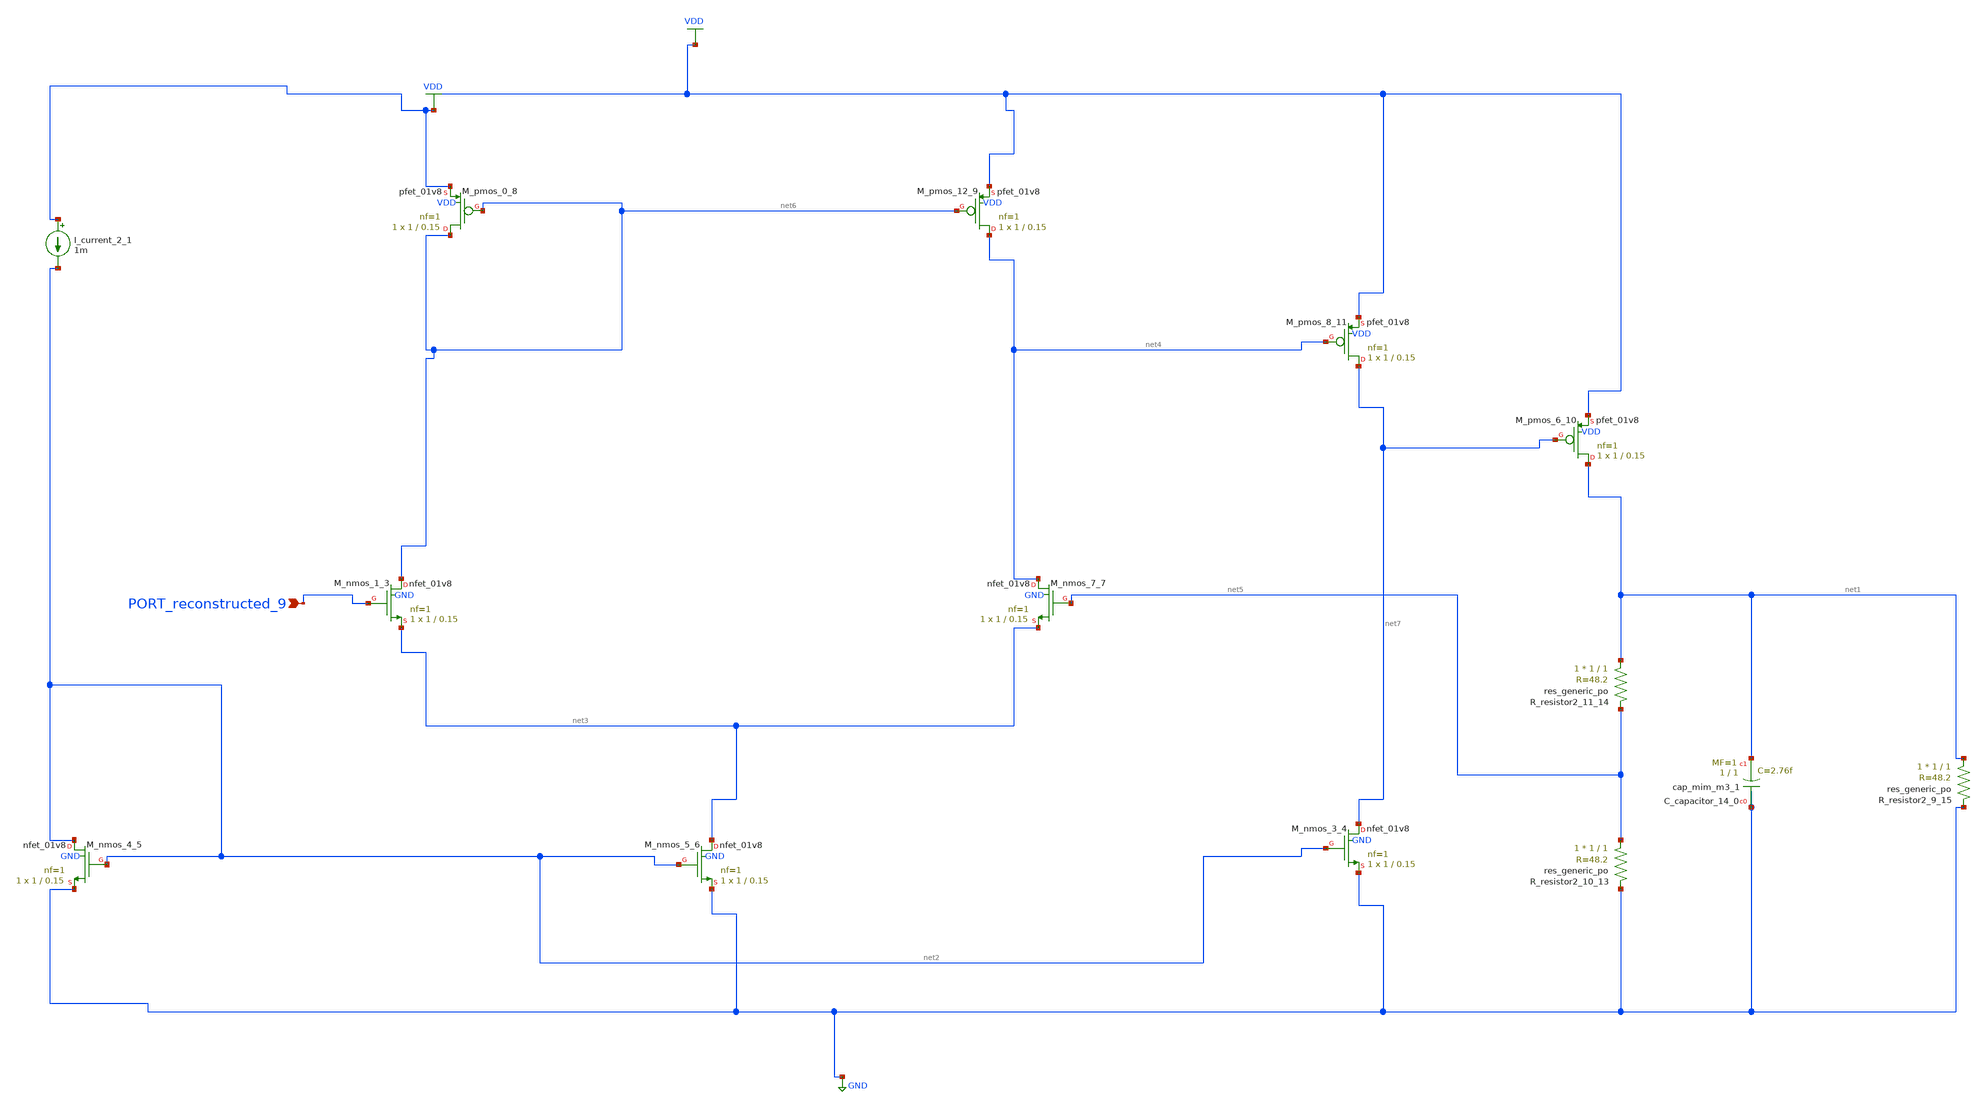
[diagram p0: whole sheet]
** sch_path: schematics/10_1007_s10470-009-9299-5_04_001_crop1.sch
**.subckt 10_1007_s10470-009-9299-5_04_001_crop1 PORT_reconstructed_9
*.ipin PORT_reconstructed_9
XC_capacitor_14_0 GND net1 sky130_fd_pr__cap_mim_m3_1 W=1 L=1 MF=1 m=1
I_current_2_1 VDD net2 1m
XM_nmos_1_3 net6 PORT_reconstructed_9 net3 GND sky130_fd_pr__nfet_01v8 L=0.15 W=1 nf=1 ad='int((1 + 1)/2) * 1 / 1 * 0.29'
+ as='int((1 + 2)/2) * 1 / 1 * 0.29' pd='2*int((1 + 1)/2) * (1 / 1 + 0.29)' ps='2*int((1 + 2)/2) * (1 / 1 + 0.29)'
+ nrd='0.29 / 1 ' nrs='0.29 / 1 ' sa=0 sb=0 sd=0 mult=1 m=1
XM_nmos_3_4 net7 net2 GND GND sky130_fd_pr__nfet_01v8 L=0.15 W=1 nf=1 ad='int((1 + 1)/2) * 1 / 1 * 0.29'
+ as='int((1 + 2)/2) * 1 / 1 * 0.29' pd='2*int((1 + 1)/2) * (1 / 1 + 0.29)' ps='2*int((1 + 2)/2) * (1 / 1 + 0.29)'
+ nrd='0.29 / 1 ' nrs='0.29 / 1 ' sa=0 sb=0 sd=0 mult=1 m=1
XM_nmos_4_5 net2 net2 GND GND sky130_fd_pr__nfet_01v8 L=0.15 W=1 nf=1 ad='int((1 + 1)/2) * 1 / 1 * 0.29'
+ as='int((1 + 2)/2) * 1 / 1 * 0.29' pd='2*int((1 + 1)/2) * (1 / 1 + 0.29)' ps='2*int((1 + 2)/2) * (1 / 1 + 0.29)'
+ nrd='0.29 / 1 ' nrs='0.29 / 1 ' sa=0 sb=0 sd=0 mult=1 m=1
XM_nmos_5_6 net3 net2 GND GND sky130_fd_pr__nfet_01v8 L=0.15 W=1 nf=1 ad='int((1 + 1)/2) * 1 / 1 * 0.29'
+ as='int((1 + 2)/2) * 1 / 1 * 0.29' pd='2*int((1 + 1)/2) * (1 / 1 + 0.29)' ps='2*int((1 + 2)/2) * (1 / 1 + 0.29)'
+ nrd='0.29 / 1 ' nrs='0.29 / 1 ' sa=0 sb=0 sd=0 mult=1 m=1
XM_nmos_7_7 net4 net5 net3 GND sky130_fd_pr__nfet_01v8 L=0.15 W=1 nf=1 ad='int((1 + 1)/2) * 1 / 1 * 0.29'
+ as='int((1 + 2)/2) * 1 / 1 * 0.29' pd='2*int((1 + 1)/2) * (1 / 1 + 0.29)' ps='2*int((1 + 2)/2) * (1 / 1 + 0.29)'
+ nrd='0.29 / 1 ' nrs='0.29 / 1 ' sa=0 sb=0 sd=0 mult=1 m=1
XM_pmos_0_8 net6 net6 VDD VDD sky130_fd_pr__pfet_01v8 L=0.15 W=1 nf=1 ad='int((1 + 1)/2) * 1 / 1 * 0.29'
+ as='int((1 + 2)/2) * 1 / 1 * 0.29' pd='2*int((1 + 1)/2) * (1 / 1 + 0.29)' ps='2*int((1 + 2)/2) * (1 / 1 + 0.29)'
+ nrd='0.29 / 1 ' nrs='0.29 / 1 ' sa=0 sb=0 sd=0 mult=1 m=1
XM_pmos_12_9 net4 net6 VDD VDD sky130_fd_pr__pfet_01v8 L=0.15 W=1 nf=1 ad='int((1 + 1)/2) * 1 / 1 * 0.29'
+ as='int((1 + 2)/2) * 1 / 1 * 0.29' pd='2*int((1 + 1)/2) * (1 / 1 + 0.29)' ps='2*int((1 + 2)/2) * (1 / 1 + 0.29)'
+ nrd='0.29 / 1 ' nrs='0.29 / 1 ' sa=0 sb=0 sd=0 mult=1 m=1
XM_pmos_6_10 net1 net7 VDD VDD sky130_fd_pr__pfet_01v8 L=0.15 W=1 nf=1 ad='int((1 + 1)/2) * 1 / 1 * 0.29'
+ as='int((1 + 2)/2) * 1 / 1 * 0.29' pd='2*int((1 + 1)/2) * (1 / 1 + 0.29)' ps='2*int((1 + 2)/2) * (1 / 1 + 0.29)'
+ nrd='0.29 / 1 ' nrs='0.29 / 1 ' sa=0 sb=0 sd=0 mult=1 m=1
XM_pmos_8_11 net7 net4 VDD VDD sky130_fd_pr__pfet_01v8 L=0.15 W=1 nf=1 ad='int((1 + 1)/2) * 1 / 1 * 0.29'
+ as='int((1 + 2)/2) * 1 / 1 * 0.29' pd='2*int((1 + 1)/2) * (1 / 1 + 0.29)' ps='2*int((1 + 2)/2) * (1 / 1 + 0.29)'
+ nrd='0.29 / 1 ' nrs='0.29 / 1 ' sa=0 sb=0 sd=0 mult=1 m=1
XR_resistor2_10_13 net5 GND sky130_fd_pr__res_generic_po W=1 L=1 m=1
XR_resistor2_11_14 net1 net5 sky130_fd_pr__res_generic_po W=1 L=1 m=1
XR_resistor2_9_15 net1 GND sky130_fd_pr__res_generic_po W=1 L=1 m=1
**.ends
.GLOBAL GND
.GLOBAL VDD
.end
